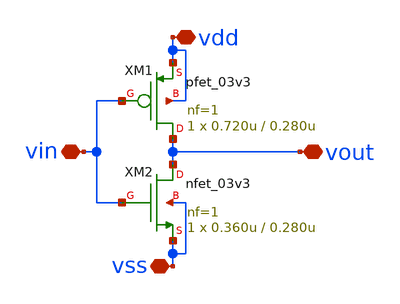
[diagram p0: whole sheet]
** sch_path: resuelto-klayout/schematic/inv.sch

.include $env(PDK_ROOT)/$env(PDK)/libs.tech/ngspice/design.ngspice

**.subckt inv vout vdd vin vss
*.iopin vout
*.iopin vdd
*.iopin vin
*.iopin vss
XM1 vout vin vdd vdd pfet_03v3 L=0.280u W=0.720u nf=1 ad='int((nf+1)/2) * W/nf * 0.18u' as='int((nf+2)/2) * W/nf * 0.18u'
+ pd='2*int((nf+1)/2) * (W/nf + 0.18u)' ps='2*int((nf+2)/2) * (W/nf + 0.18u)' nrd='0.18u / W' nrs='0.18u / W'
+ sa=0 sb=0 sd=0 m=1
XM2 vout vin vss vss nfet_03v3 L=0.280u W=0.360u nf=1 ad='int((nf+1)/2) * W/nf * 0.18u' as='int((nf+2)/2) * W/nf * 0.18u'
+ pd='2*int((nf+1)/2) * (W/nf + 0.18u)' ps='2*int((nf+2)/2) * (W/nf + 0.18u)' nrd='0.18u / W' nrs='0.18u / W'
+ sa=0 sb=0 sd=0 m=1
**.ends
.end
